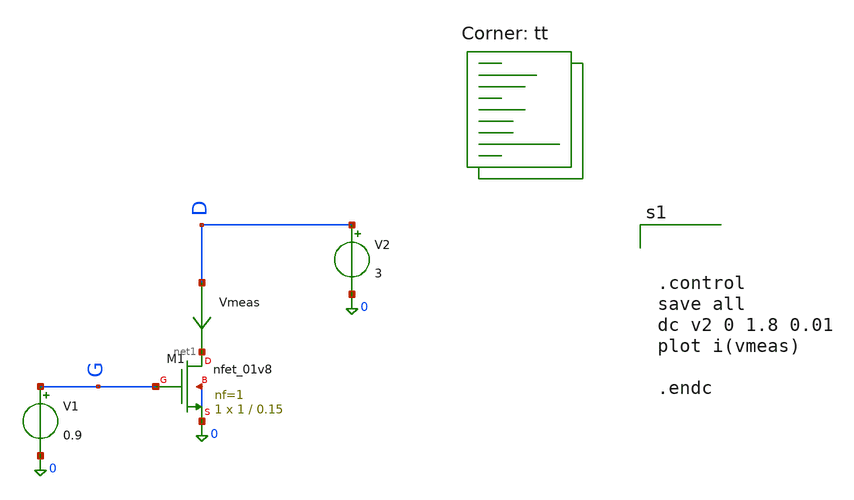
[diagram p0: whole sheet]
** sch_path: Training-3/tes.sch
**.subckt tes
XM1 net1 G 0 0 sky130_fd_pr__nfet_01v8 L=0.15 W=1 nf=1 ad='int((nf+1)/2) * W/nf * 0.29' as='int((nf+2)/2) * W/nf * 0.29'
+ pd='2*int((nf+1)/2) * (W/nf + 0.29)' ps='2*int((nf+2)/2) * (W/nf + 0.29)' nrd='0.29 / W' nrs='0.29 / W'
+ sa=0 sb=0 sd=0 mult=1 m=1
Vmeas D net1 0
.save i(vmeas)
V1 G 0 0.9
V2 D 0 3
**** begin user architecture code
.lib $::SKYWATER_MODELS/sky130.lib.spice tt



.control
save all
dc v2 0 1.8 0.01
plot i(vmeas)

.endc





**** end user architecture code
**.ends
.end
